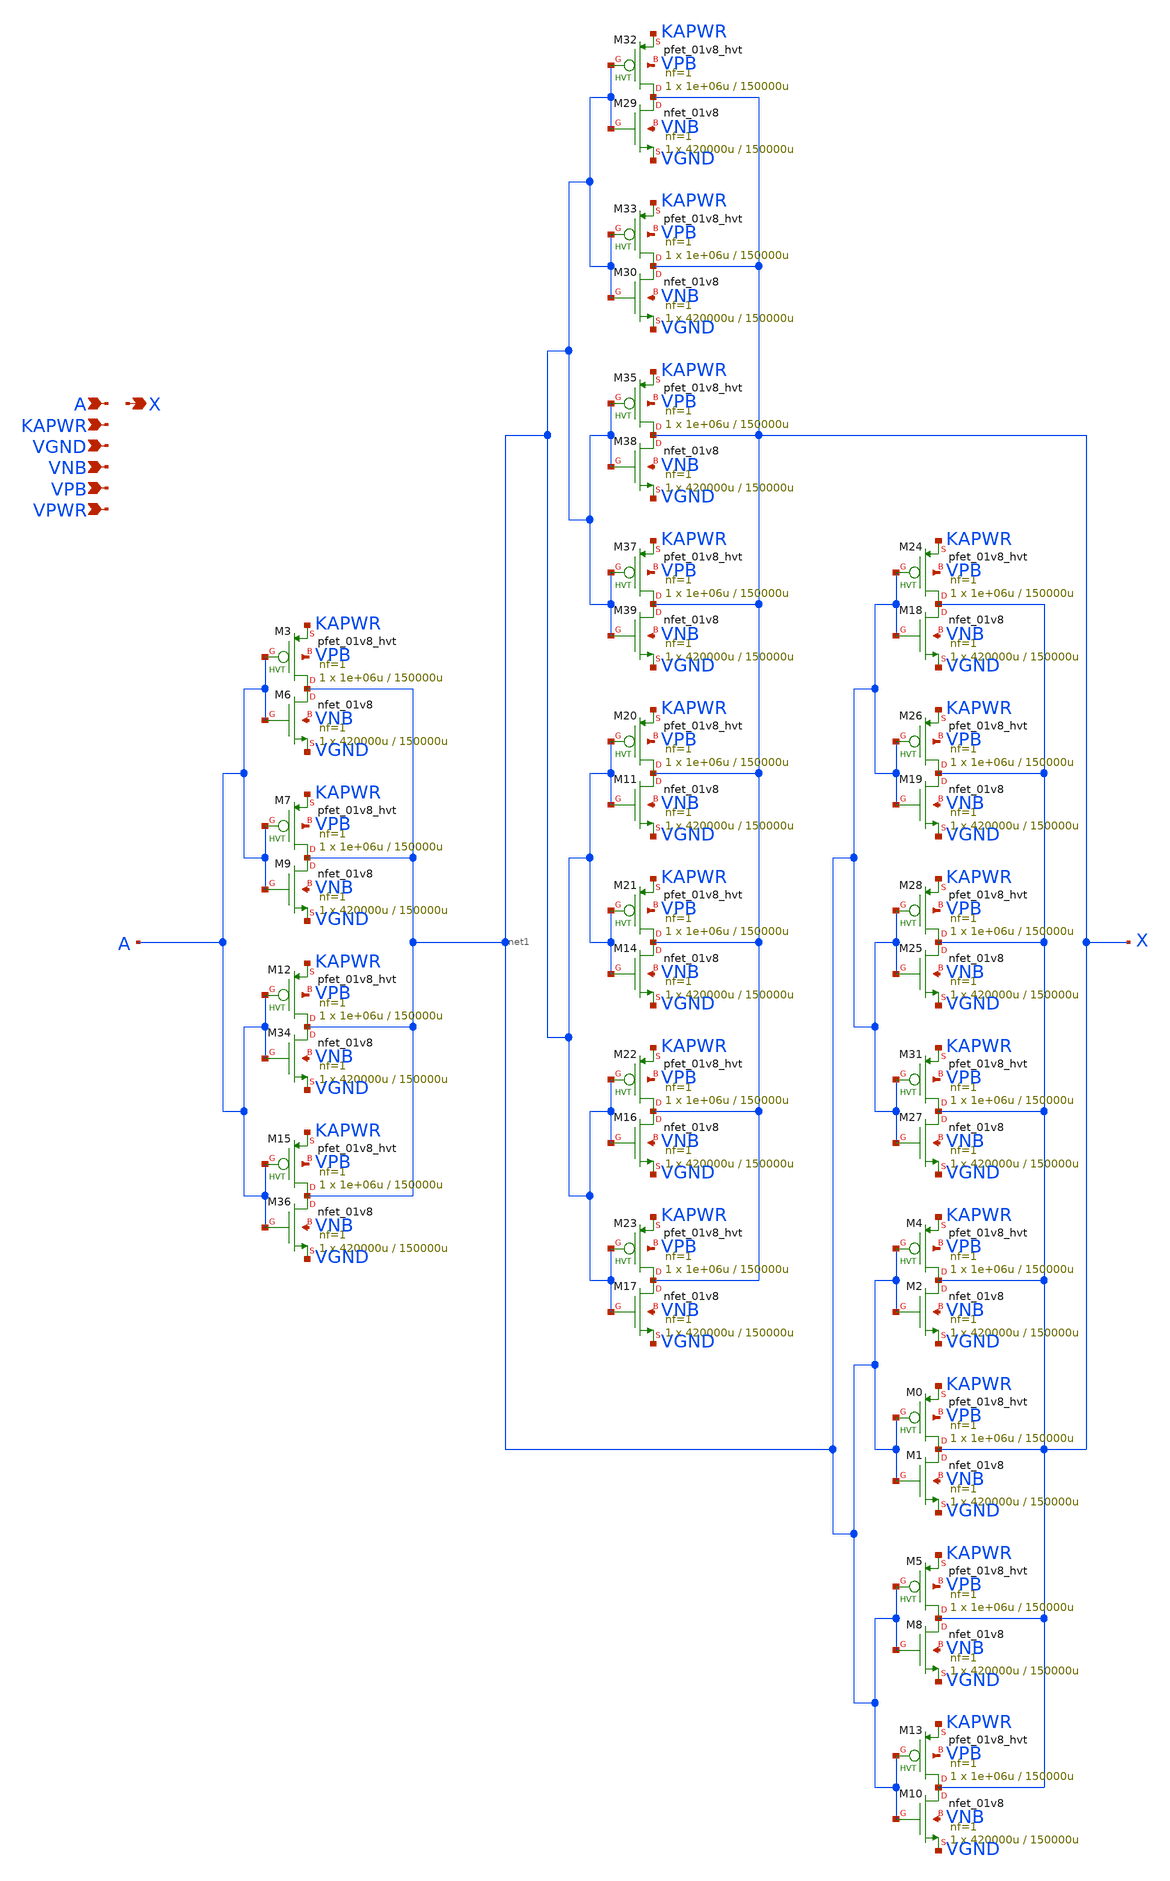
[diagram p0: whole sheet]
** sch_path: schematics/lpflow_clkbufkapwr/sky130_fd_sc_hd__lpflow_clkbufkapwr_16.sch
**.subckt sky130_fd_sc_hd__lpflow_clkbufkapwr_16 A KAPWR VGND VNB VPB VPWR X
*.ipin A
*.ipin KAPWR
*.ipin VGND
*.ipin VNB
*.ipin VPB
*.ipin VPWR
*.opin X
XM3 net1 A KAPWR VPB sky130_fd_pr__pfet_01v8_hvt L=150000u W=1e+06u nf=1 ad='int((1 + 1)/2) * 1e+06u / 1 * 0.29'
+ as='int((1 + 2)/2) * 1e+06u / 1 * 0.29' pd='2*int((1 + 1)/2) * (1e+06u / 1 + 0.29)' ps='2*int((1 + 2)/2) * (1e+06u / 1 + 0.29)'
+ nrd='0.29 / 1e+06u ' nrs='0.29 / 1e+06u ' sa=0 sb=0 sd=0 mult=1 m=1
XM7 net1 A KAPWR VPB sky130_fd_pr__pfet_01v8_hvt L=150000u W=1e+06u nf=1 ad='int((1 + 1)/2) * 1e+06u / 1 * 0.29'
+ as='int((1 + 2)/2) * 1e+06u / 1 * 0.29' pd='2*int((1 + 1)/2) * (1e+06u / 1 + 0.29)' ps='2*int((1 + 2)/2) * (1e+06u / 1 + 0.29)'
+ nrd='0.29 / 1e+06u ' nrs='0.29 / 1e+06u ' sa=0 sb=0 sd=0 mult=1 m=1
XM12 net1 A KAPWR VPB sky130_fd_pr__pfet_01v8_hvt L=150000u W=1e+06u nf=1 ad='int((1 + 1)/2) * 1e+06u / 1 * 0.29'
+ as='int((1 + 2)/2) * 1e+06u / 1 * 0.29' pd='2*int((1 + 1)/2) * (1e+06u / 1 + 0.29)' ps='2*int((1 + 2)/2) * (1e+06u / 1 + 0.29)'
+ nrd='0.29 / 1e+06u ' nrs='0.29 / 1e+06u ' sa=0 sb=0 sd=0 mult=1 m=1
XM15 net1 A KAPWR VPB sky130_fd_pr__pfet_01v8_hvt L=150000u W=1e+06u nf=1 ad='int((1 + 1)/2) * 1e+06u / 1 * 0.29'
+ as='int((1 + 2)/2) * 1e+06u / 1 * 0.29' pd='2*int((1 + 1)/2) * (1e+06u / 1 + 0.29)' ps='2*int((1 + 2)/2) * (1e+06u / 1 + 0.29)'
+ nrd='0.29 / 1e+06u ' nrs='0.29 / 1e+06u ' sa=0 sb=0 sd=0 mult=1 m=1
XM0 X net1 KAPWR VPB sky130_fd_pr__pfet_01v8_hvt L=150000u W=1e+06u nf=1 ad='int((1 + 1)/2) * 1e+06u / 1 * 0.29'
+ as='int((1 + 2)/2) * 1e+06u / 1 * 0.29' pd='2*int((1 + 1)/2) * (1e+06u / 1 + 0.29)' ps='2*int((1 + 2)/2) * (1e+06u / 1 + 0.29)'
+ nrd='0.29 / 1e+06u ' nrs='0.29 / 1e+06u ' sa=0 sb=0 sd=0 mult=1 m=1
XM4 X net1 KAPWR VPB sky130_fd_pr__pfet_01v8_hvt L=150000u W=1e+06u nf=1 ad='int((1 + 1)/2) * 1e+06u / 1 * 0.29'
+ as='int((1 + 2)/2) * 1e+06u / 1 * 0.29' pd='2*int((1 + 1)/2) * (1e+06u / 1 + 0.29)' ps='2*int((1 + 2)/2) * (1e+06u / 1 + 0.29)'
+ nrd='0.29 / 1e+06u ' nrs='0.29 / 1e+06u ' sa=0 sb=0 sd=0 mult=1 m=1
XM5 X net1 KAPWR VPB sky130_fd_pr__pfet_01v8_hvt L=150000u W=1e+06u nf=1 ad='int((1 + 1)/2) * 1e+06u / 1 * 0.29'
+ as='int((1 + 2)/2) * 1e+06u / 1 * 0.29' pd='2*int((1 + 1)/2) * (1e+06u / 1 + 0.29)' ps='2*int((1 + 2)/2) * (1e+06u / 1 + 0.29)'
+ nrd='0.29 / 1e+06u ' nrs='0.29 / 1e+06u ' sa=0 sb=0 sd=0 mult=1 m=1
XM13 X net1 KAPWR VPB sky130_fd_pr__pfet_01v8_hvt L=150000u W=1e+06u nf=1 ad='int((1 + 1)/2) * 1e+06u / 1 * 0.29'
+ as='int((1 + 2)/2) * 1e+06u / 1 * 0.29' pd='2*int((1 + 1)/2) * (1e+06u / 1 + 0.29)' ps='2*int((1 + 2)/2) * (1e+06u / 1 + 0.29)'
+ nrd='0.29 / 1e+06u ' nrs='0.29 / 1e+06u ' sa=0 sb=0 sd=0 mult=1 m=1
XM20 X net1 KAPWR VPB sky130_fd_pr__pfet_01v8_hvt L=150000u W=1e+06u nf=1 ad='int((1 + 1)/2) * 1e+06u / 1 * 0.29'
+ as='int((1 + 2)/2) * 1e+06u / 1 * 0.29' pd='2*int((1 + 1)/2) * (1e+06u / 1 + 0.29)' ps='2*int((1 + 2)/2) * (1e+06u / 1 + 0.29)'
+ nrd='0.29 / 1e+06u ' nrs='0.29 / 1e+06u ' sa=0 sb=0 sd=0 mult=1 m=1
XM21 X net1 KAPWR VPB sky130_fd_pr__pfet_01v8_hvt L=150000u W=1e+06u nf=1 ad='int((1 + 1)/2) * 1e+06u / 1 * 0.29'
+ as='int((1 + 2)/2) * 1e+06u / 1 * 0.29' pd='2*int((1 + 1)/2) * (1e+06u / 1 + 0.29)' ps='2*int((1 + 2)/2) * (1e+06u / 1 + 0.29)'
+ nrd='0.29 / 1e+06u ' nrs='0.29 / 1e+06u ' sa=0 sb=0 sd=0 mult=1 m=1
XM22 X net1 KAPWR VPB sky130_fd_pr__pfet_01v8_hvt L=150000u W=1e+06u nf=1 ad='int((1 + 1)/2) * 1e+06u / 1 * 0.29'
+ as='int((1 + 2)/2) * 1e+06u / 1 * 0.29' pd='2*int((1 + 1)/2) * (1e+06u / 1 + 0.29)' ps='2*int((1 + 2)/2) * (1e+06u / 1 + 0.29)'
+ nrd='0.29 / 1e+06u ' nrs='0.29 / 1e+06u ' sa=0 sb=0 sd=0 mult=1 m=1
XM23 X net1 KAPWR VPB sky130_fd_pr__pfet_01v8_hvt L=150000u W=1e+06u nf=1 ad='int((1 + 1)/2) * 1e+06u / 1 * 0.29'
+ as='int((1 + 2)/2) * 1e+06u / 1 * 0.29' pd='2*int((1 + 1)/2) * (1e+06u / 1 + 0.29)' ps='2*int((1 + 2)/2) * (1e+06u / 1 + 0.29)'
+ nrd='0.29 / 1e+06u ' nrs='0.29 / 1e+06u ' sa=0 sb=0 sd=0 mult=1 m=1
XM24 X net1 KAPWR VPB sky130_fd_pr__pfet_01v8_hvt L=150000u W=1e+06u nf=1 ad='int((1 + 1)/2) * 1e+06u / 1 * 0.29'
+ as='int((1 + 2)/2) * 1e+06u / 1 * 0.29' pd='2*int((1 + 1)/2) * (1e+06u / 1 + 0.29)' ps='2*int((1 + 2)/2) * (1e+06u / 1 + 0.29)'
+ nrd='0.29 / 1e+06u ' nrs='0.29 / 1e+06u ' sa=0 sb=0 sd=0 mult=1 m=1
XM26 X net1 KAPWR VPB sky130_fd_pr__pfet_01v8_hvt L=150000u W=1e+06u nf=1 ad='int((1 + 1)/2) * 1e+06u / 1 * 0.29'
+ as='int((1 + 2)/2) * 1e+06u / 1 * 0.29' pd='2*int((1 + 1)/2) * (1e+06u / 1 + 0.29)' ps='2*int((1 + 2)/2) * (1e+06u / 1 + 0.29)'
+ nrd='0.29 / 1e+06u ' nrs='0.29 / 1e+06u ' sa=0 sb=0 sd=0 mult=1 m=1
XM28 X net1 KAPWR VPB sky130_fd_pr__pfet_01v8_hvt L=150000u W=1e+06u nf=1 ad='int((1 + 1)/2) * 1e+06u / 1 * 0.29'
+ as='int((1 + 2)/2) * 1e+06u / 1 * 0.29' pd='2*int((1 + 1)/2) * (1e+06u / 1 + 0.29)' ps='2*int((1 + 2)/2) * (1e+06u / 1 + 0.29)'
+ nrd='0.29 / 1e+06u ' nrs='0.29 / 1e+06u ' sa=0 sb=0 sd=0 mult=1 m=1
XM31 X net1 KAPWR VPB sky130_fd_pr__pfet_01v8_hvt L=150000u W=1e+06u nf=1 ad='int((1 + 1)/2) * 1e+06u / 1 * 0.29'
+ as='int((1 + 2)/2) * 1e+06u / 1 * 0.29' pd='2*int((1 + 1)/2) * (1e+06u / 1 + 0.29)' ps='2*int((1 + 2)/2) * (1e+06u / 1 + 0.29)'
+ nrd='0.29 / 1e+06u ' nrs='0.29 / 1e+06u ' sa=0 sb=0 sd=0 mult=1 m=1
XM32 X net1 KAPWR VPB sky130_fd_pr__pfet_01v8_hvt L=150000u W=1e+06u nf=1 ad='int((1 + 1)/2) * 1e+06u / 1 * 0.29'
+ as='int((1 + 2)/2) * 1e+06u / 1 * 0.29' pd='2*int((1 + 1)/2) * (1e+06u / 1 + 0.29)' ps='2*int((1 + 2)/2) * (1e+06u / 1 + 0.29)'
+ nrd='0.29 / 1e+06u ' nrs='0.29 / 1e+06u ' sa=0 sb=0 sd=0 mult=1 m=1
XM33 X net1 KAPWR VPB sky130_fd_pr__pfet_01v8_hvt L=150000u W=1e+06u nf=1 ad='int((1 + 1)/2) * 1e+06u / 1 * 0.29'
+ as='int((1 + 2)/2) * 1e+06u / 1 * 0.29' pd='2*int((1 + 1)/2) * (1e+06u / 1 + 0.29)' ps='2*int((1 + 2)/2) * (1e+06u / 1 + 0.29)'
+ nrd='0.29 / 1e+06u ' nrs='0.29 / 1e+06u ' sa=0 sb=0 sd=0 mult=1 m=1
XM35 X net1 KAPWR VPB sky130_fd_pr__pfet_01v8_hvt L=150000u W=1e+06u nf=1 ad='int((1 + 1)/2) * 1e+06u / 1 * 0.29'
+ as='int((1 + 2)/2) * 1e+06u / 1 * 0.29' pd='2*int((1 + 1)/2) * (1e+06u / 1 + 0.29)' ps='2*int((1 + 2)/2) * (1e+06u / 1 + 0.29)'
+ nrd='0.29 / 1e+06u ' nrs='0.29 / 1e+06u ' sa=0 sb=0 sd=0 mult=1 m=1
XM37 X net1 KAPWR VPB sky130_fd_pr__pfet_01v8_hvt L=150000u W=1e+06u nf=1 ad='int((1 + 1)/2) * 1e+06u / 1 * 0.29'
+ as='int((1 + 2)/2) * 1e+06u / 1 * 0.29' pd='2*int((1 + 1)/2) * (1e+06u / 1 + 0.29)' ps='2*int((1 + 2)/2) * (1e+06u / 1 + 0.29)'
+ nrd='0.29 / 1e+06u ' nrs='0.29 / 1e+06u ' sa=0 sb=0 sd=0 mult=1 m=1
XM6 net1 A VGND VNB sky130_fd_pr__nfet_01v8 L=150000u W=420000u nf=1 ad='int((1 + 1)/2) * 420000u / 1 * 0.29'
+ as='int((1 + 2)/2) * 420000u / 1 * 0.29' pd='2*int((1 + 1)/2) * (420000u / 1 + 0.29)' ps='2*int((1 + 2)/2) * (420000u / 1 + 0.29)'
+ nrd='0.29 / 420000u ' nrs='0.29 / 420000u ' sa=0 sb=0 sd=0 mult=1 m=1
XM9 net1 A VGND VNB sky130_fd_pr__nfet_01v8 L=150000u W=420000u nf=1 ad='int((1 + 1)/2) * 420000u / 1 * 0.29'
+ as='int((1 + 2)/2) * 420000u / 1 * 0.29' pd='2*int((1 + 1)/2) * (420000u / 1 + 0.29)' ps='2*int((1 + 2)/2) * (420000u / 1 + 0.29)'
+ nrd='0.29 / 420000u ' nrs='0.29 / 420000u ' sa=0 sb=0 sd=0 mult=1 m=1
XM34 net1 A VGND VNB sky130_fd_pr__nfet_01v8 L=150000u W=420000u nf=1 ad='int((1 + 1)/2) * 420000u / 1 * 0.29'
+ as='int((1 + 2)/2) * 420000u / 1 * 0.29' pd='2*int((1 + 1)/2) * (420000u / 1 + 0.29)' ps='2*int((1 + 2)/2) * (420000u / 1 + 0.29)'
+ nrd='0.29 / 420000u ' nrs='0.29 / 420000u ' sa=0 sb=0 sd=0 mult=1 m=1
XM36 net1 A VGND VNB sky130_fd_pr__nfet_01v8 L=150000u W=420000u nf=1 ad='int((1 + 1)/2) * 420000u / 1 * 0.29'
+ as='int((1 + 2)/2) * 420000u / 1 * 0.29' pd='2*int((1 + 1)/2) * (420000u / 1 + 0.29)' ps='2*int((1 + 2)/2) * (420000u / 1 + 0.29)'
+ nrd='0.29 / 420000u ' nrs='0.29 / 420000u ' sa=0 sb=0 sd=0 mult=1 m=1
XM1 X net1 VGND VNB sky130_fd_pr__nfet_01v8 L=150000u W=420000u nf=1 ad='int((1 + 1)/2) * 420000u / 1 * 0.29'
+ as='int((1 + 2)/2) * 420000u / 1 * 0.29' pd='2*int((1 + 1)/2) * (420000u / 1 + 0.29)' ps='2*int((1 + 2)/2) * (420000u / 1 + 0.29)'
+ nrd='0.29 / 420000u ' nrs='0.29 / 420000u ' sa=0 sb=0 sd=0 mult=1 m=1
XM2 X net1 VGND VNB sky130_fd_pr__nfet_01v8 L=150000u W=420000u nf=1 ad='int((1 + 1)/2) * 420000u / 1 * 0.29'
+ as='int((1 + 2)/2) * 420000u / 1 * 0.29' pd='2*int((1 + 1)/2) * (420000u / 1 + 0.29)' ps='2*int((1 + 2)/2) * (420000u / 1 + 0.29)'
+ nrd='0.29 / 420000u ' nrs='0.29 / 420000u ' sa=0 sb=0 sd=0 mult=1 m=1
XM8 X net1 VGND VNB sky130_fd_pr__nfet_01v8 L=150000u W=420000u nf=1 ad='int((1 + 1)/2) * 420000u / 1 * 0.29'
+ as='int((1 + 2)/2) * 420000u / 1 * 0.29' pd='2*int((1 + 1)/2) * (420000u / 1 + 0.29)' ps='2*int((1 + 2)/2) * (420000u / 1 + 0.29)'
+ nrd='0.29 / 420000u ' nrs='0.29 / 420000u ' sa=0 sb=0 sd=0 mult=1 m=1
XM10 X net1 VGND VNB sky130_fd_pr__nfet_01v8 L=150000u W=420000u nf=1 ad='int((1 + 1)/2) * 420000u / 1 * 0.29'
+ as='int((1 + 2)/2) * 420000u / 1 * 0.29' pd='2*int((1 + 1)/2) * (420000u / 1 + 0.29)' ps='2*int((1 + 2)/2) * (420000u / 1 + 0.29)'
+ nrd='0.29 / 420000u ' nrs='0.29 / 420000u ' sa=0 sb=0 sd=0 mult=1 m=1
XM11 X net1 VGND VNB sky130_fd_pr__nfet_01v8 L=150000u W=420000u nf=1 ad='int((1 + 1)/2) * 420000u / 1 * 0.29'
+ as='int((1 + 2)/2) * 420000u / 1 * 0.29' pd='2*int((1 + 1)/2) * (420000u / 1 + 0.29)' ps='2*int((1 + 2)/2) * (420000u / 1 + 0.29)'
+ nrd='0.29 / 420000u ' nrs='0.29 / 420000u ' sa=0 sb=0 sd=0 mult=1 m=1
XM14 X net1 VGND VNB sky130_fd_pr__nfet_01v8 L=150000u W=420000u nf=1 ad='int((1 + 1)/2) * 420000u / 1 * 0.29'
+ as='int((1 + 2)/2) * 420000u / 1 * 0.29' pd='2*int((1 + 1)/2) * (420000u / 1 + 0.29)' ps='2*int((1 + 2)/2) * (420000u / 1 + 0.29)'
+ nrd='0.29 / 420000u ' nrs='0.29 / 420000u ' sa=0 sb=0 sd=0 mult=1 m=1
XM16 X net1 VGND VNB sky130_fd_pr__nfet_01v8 L=150000u W=420000u nf=1 ad='int((1 + 1)/2) * 420000u / 1 * 0.29'
+ as='int((1 + 2)/2) * 420000u / 1 * 0.29' pd='2*int((1 + 1)/2) * (420000u / 1 + 0.29)' ps='2*int((1 + 2)/2) * (420000u / 1 + 0.29)'
+ nrd='0.29 / 420000u ' nrs='0.29 / 420000u ' sa=0 sb=0 sd=0 mult=1 m=1
XM17 X net1 VGND VNB sky130_fd_pr__nfet_01v8 L=150000u W=420000u nf=1 ad='int((1 + 1)/2) * 420000u / 1 * 0.29'
+ as='int((1 + 2)/2) * 420000u / 1 * 0.29' pd='2*int((1 + 1)/2) * (420000u / 1 + 0.29)' ps='2*int((1 + 2)/2) * (420000u / 1 + 0.29)'
+ nrd='0.29 / 420000u ' nrs='0.29 / 420000u ' sa=0 sb=0 sd=0 mult=1 m=1
XM18 X net1 VGND VNB sky130_fd_pr__nfet_01v8 L=150000u W=420000u nf=1 ad='int((1 + 1)/2) * 420000u / 1 * 0.29'
+ as='int((1 + 2)/2) * 420000u / 1 * 0.29' pd='2*int((1 + 1)/2) * (420000u / 1 + 0.29)' ps='2*int((1 + 2)/2) * (420000u / 1 + 0.29)'
+ nrd='0.29 / 420000u ' nrs='0.29 / 420000u ' sa=0 sb=0 sd=0 mult=1 m=1
XM19 X net1 VGND VNB sky130_fd_pr__nfet_01v8 L=150000u W=420000u nf=1 ad='int((1 + 1)/2) * 420000u / 1 * 0.29'
+ as='int((1 + 2)/2) * 420000u / 1 * 0.29' pd='2*int((1 + 1)/2) * (420000u / 1 + 0.29)' ps='2*int((1 + 2)/2) * (420000u / 1 + 0.29)'
+ nrd='0.29 / 420000u ' nrs='0.29 / 420000u ' sa=0 sb=0 sd=0 mult=1 m=1
XM25 X net1 VGND VNB sky130_fd_pr__nfet_01v8 L=150000u W=420000u nf=1 ad='int((1 + 1)/2) * 420000u / 1 * 0.29'
+ as='int((1 + 2)/2) * 420000u / 1 * 0.29' pd='2*int((1 + 1)/2) * (420000u / 1 + 0.29)' ps='2*int((1 + 2)/2) * (420000u / 1 + 0.29)'
+ nrd='0.29 / 420000u ' nrs='0.29 / 420000u ' sa=0 sb=0 sd=0 mult=1 m=1
XM27 X net1 VGND VNB sky130_fd_pr__nfet_01v8 L=150000u W=420000u nf=1 ad='int((1 + 1)/2) * 420000u / 1 * 0.29'
+ as='int((1 + 2)/2) * 420000u / 1 * 0.29' pd='2*int((1 + 1)/2) * (420000u / 1 + 0.29)' ps='2*int((1 + 2)/2) * (420000u / 1 + 0.29)'
+ nrd='0.29 / 420000u ' nrs='0.29 / 420000u ' sa=0 sb=0 sd=0 mult=1 m=1
XM29 X net1 VGND VNB sky130_fd_pr__nfet_01v8 L=150000u W=420000u nf=1 ad='int((1 + 1)/2) * 420000u / 1 * 0.29'
+ as='int((1 + 2)/2) * 420000u / 1 * 0.29' pd='2*int((1 + 1)/2) * (420000u / 1 + 0.29)' ps='2*int((1 + 2)/2) * (420000u / 1 + 0.29)'
+ nrd='0.29 / 420000u ' nrs='0.29 / 420000u ' sa=0 sb=0 sd=0 mult=1 m=1
XM30 X net1 VGND VNB sky130_fd_pr__nfet_01v8 L=150000u W=420000u nf=1 ad='int((1 + 1)/2) * 420000u / 1 * 0.29'
+ as='int((1 + 2)/2) * 420000u / 1 * 0.29' pd='2*int((1 + 1)/2) * (420000u / 1 + 0.29)' ps='2*int((1 + 2)/2) * (420000u / 1 + 0.29)'
+ nrd='0.29 / 420000u ' nrs='0.29 / 420000u ' sa=0 sb=0 sd=0 mult=1 m=1
XM38 X net1 VGND VNB sky130_fd_pr__nfet_01v8 L=150000u W=420000u nf=1 ad='int((1 + 1)/2) * 420000u / 1 * 0.29'
+ as='int((1 + 2)/2) * 420000u / 1 * 0.29' pd='2*int((1 + 1)/2) * (420000u / 1 + 0.29)' ps='2*int((1 + 2)/2) * (420000u / 1 + 0.29)'
+ nrd='0.29 / 420000u ' nrs='0.29 / 420000u ' sa=0 sb=0 sd=0 mult=1 m=1
XM39 X net1 VGND VNB sky130_fd_pr__nfet_01v8 L=150000u W=420000u nf=1 ad='int((1 + 1)/2) * 420000u / 1 * 0.29'
+ as='int((1 + 2)/2) * 420000u / 1 * 0.29' pd='2*int((1 + 1)/2) * (420000u / 1 + 0.29)' ps='2*int((1 + 2)/2) * (420000u / 1 + 0.29)'
+ nrd='0.29 / 420000u ' nrs='0.29 / 420000u ' sa=0 sb=0 sd=0 mult=1 m=1
**.ends
.end
